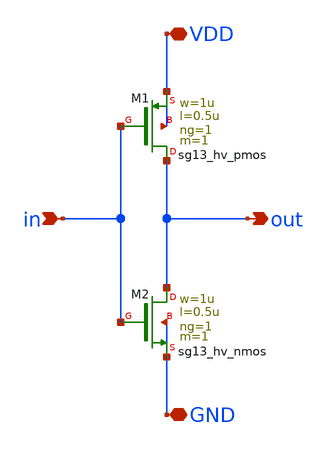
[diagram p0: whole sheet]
** sch_path: xschem/inv.sch
**.subckt inv in VDD GND out
*.ipin in
*.iopin VDD
*.iopin GND
*.opin out
XM1 out in VDD VDD sg13_hv_pmos w=1u l=0.5u ng=1 m=1 mm_ok=1
XM2 out in GND GND sg13_hv_nmos w=1u l=0.5u ng=1 m=1 mm_ok=1
**.ends
.end
